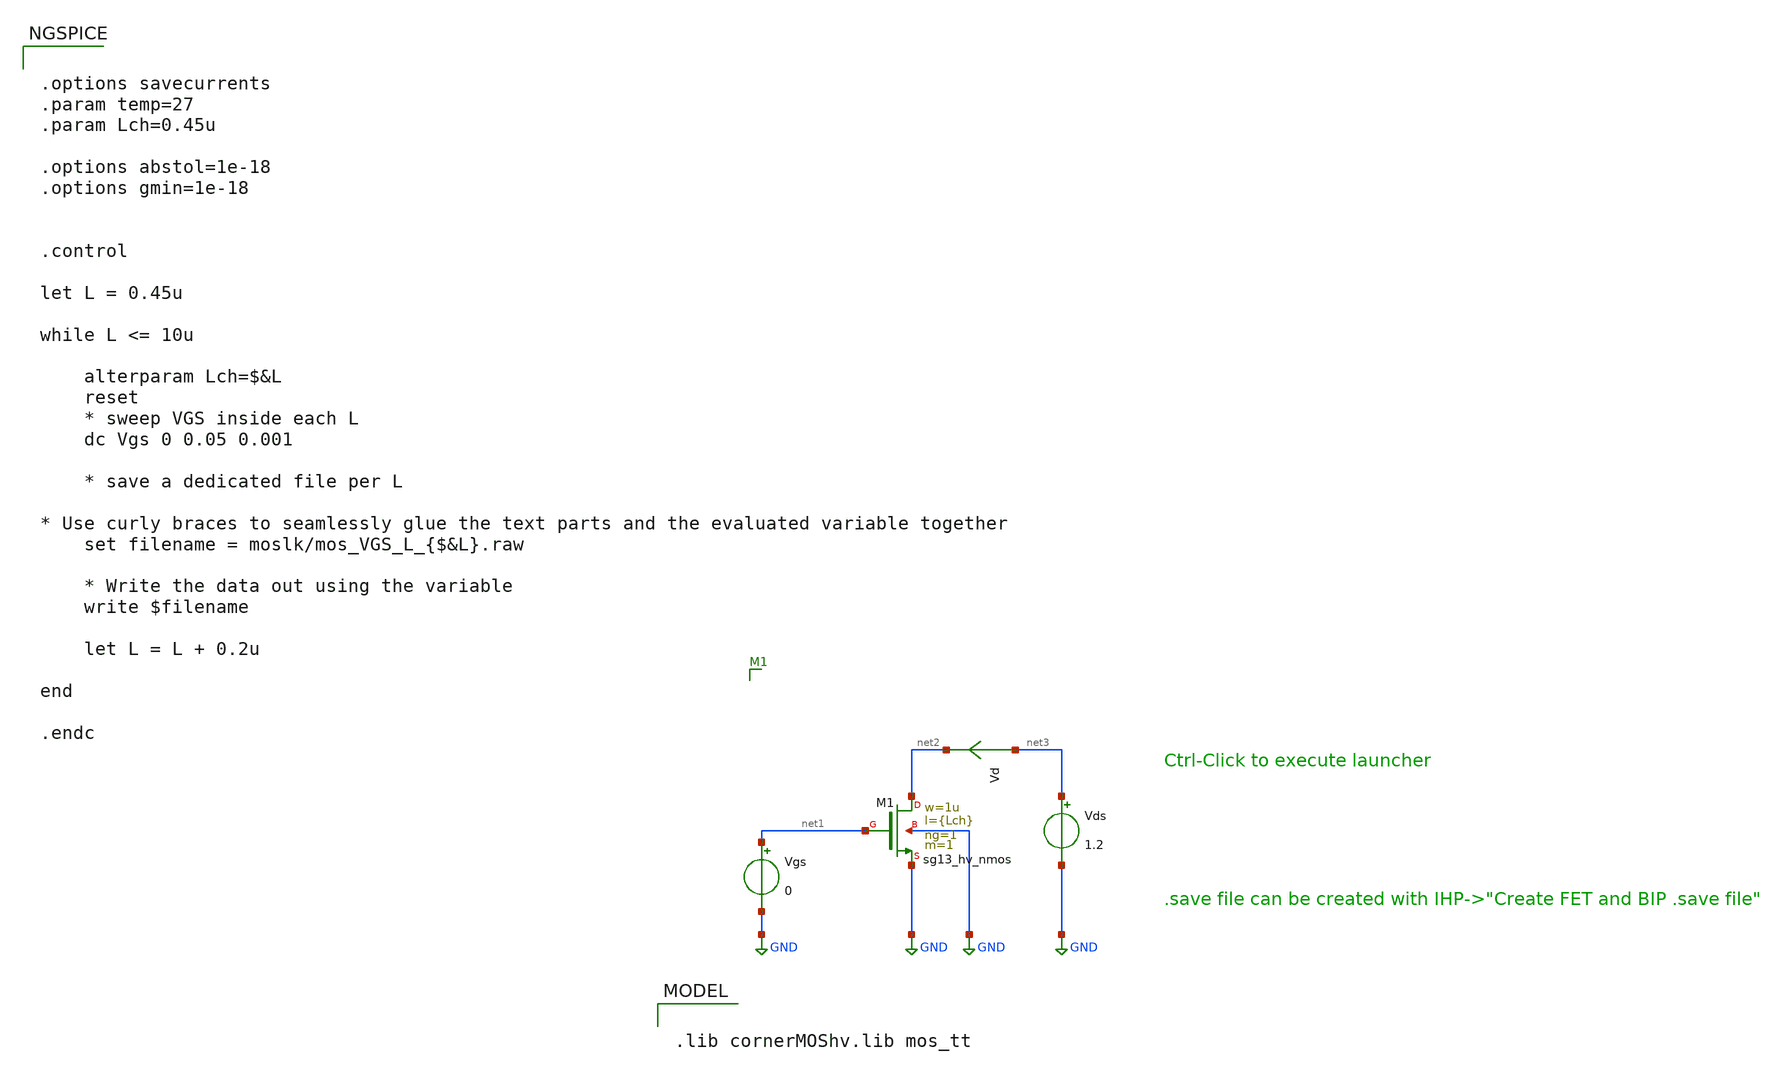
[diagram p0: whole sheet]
** sch_path: test_bench/nmosLeak_cara_op_tb.sch
* Copyright 2023 IHP PDK Authors
**.subckt nmosLeak_cara_op_tb
Vgs net1 GND 0
Vds net3 GND 1.2
Vd net3 net2 0
.save i(vd)
XM1 net2 net1 GND GND sg13_hv_nmos w=1u l={Lch} ng=1 m=1 mm_ok=1
**** begin user architecture code

.lib cornerMOShv.lib mos_tt



.options savecurrents
.param temp=27
.param Lch=0.45u

.options abstol=1e-18
.options gmin=1e-18


.control

let L = 0.45u

while L <= 10u

    alterparam Lch=$&L
    reset
    * sweep VGS inside each L
    dc Vgs 0 0.05 0.001

    * save a dedicated file per L

* Use curly braces to seamlessly glue the text parts and the evaluated variable together
    set filename = moslk/mos_VGS_L_{$&L}.raw

    * Write the data out using the variable
    write $filename

    let L = L + 0.2u

end

.endc


**** end user architecture code
**.ends
.GLOBAL GND
.end
